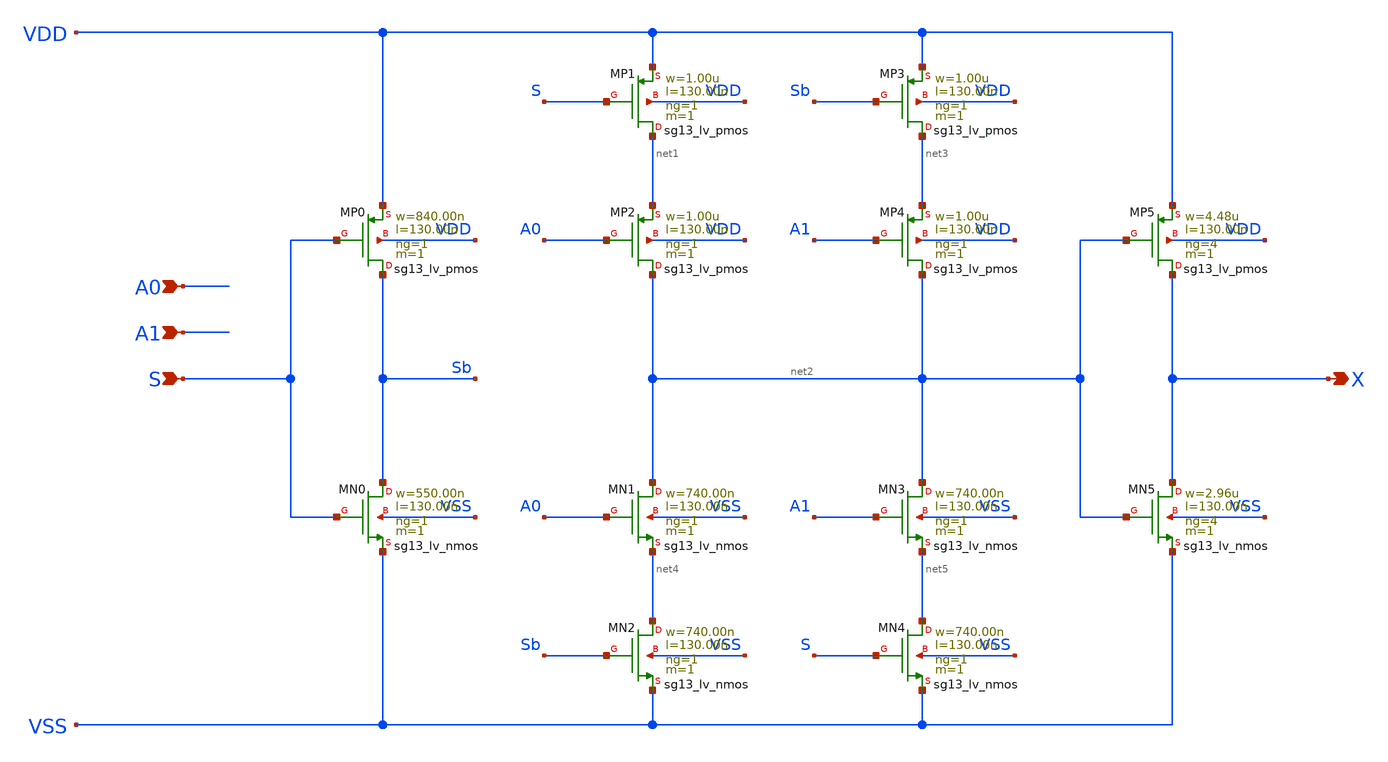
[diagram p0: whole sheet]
** sch_path: outputs/sg13g2_cells/cells/sg13g2_mux2_4/sg13g2_mux2_4.sch
**.subckt sg13g2_mux2_4 A0 A1 S X
*.ipin A0
*.ipin A1
*.ipin S
*.opin X
XMN1 net2 A0 net4 VSS sg13_lv_nmos w=740.00n l=130.00n ng=1 m=1 mm_ok=1
XMN2 net4 Sb VSS VSS sg13_lv_nmos w=740.00n l=130.00n ng=1 m=1 mm_ok=1
XMN3 net2 A1 net5 VSS sg13_lv_nmos w=740.00n l=130.00n ng=1 m=1 mm_ok=1
XMN4 net5 S VSS VSS sg13_lv_nmos w=740.00n l=130.00n ng=1 m=1 mm_ok=1
XMN0 Sb S VSS VSS sg13_lv_nmos w=550.00n l=130.00n ng=1 m=1 mm_ok=1
XMN5 X net2 VSS VSS sg13_lv_nmos w=2.96u l=130.00n ng=4 m=1 mm_ok=1
XMP1 net1 S VDD VDD sg13_lv_pmos w=1.00u l=130.00n ng=1 m=1 mm_ok=1
XMP2 net2 A0 net1 VDD sg13_lv_pmos w=1.00u l=130.00n ng=1 m=1 mm_ok=1
XMP3 net3 Sb VDD VDD sg13_lv_pmos w=1.00u l=130.00n ng=1 m=1 mm_ok=1
XMP4 net2 A1 net3 VDD sg13_lv_pmos w=1.00u l=130.00n ng=1 m=1 mm_ok=1
XMP5 X net2 VDD VDD sg13_lv_pmos w=4.48u l=130.00n ng=4 m=1 mm_ok=1
XMP0 Sb S VDD VDD sg13_lv_pmos w=840.00n l=130.00n ng=1 m=1 mm_ok=1
**.ends
.end
